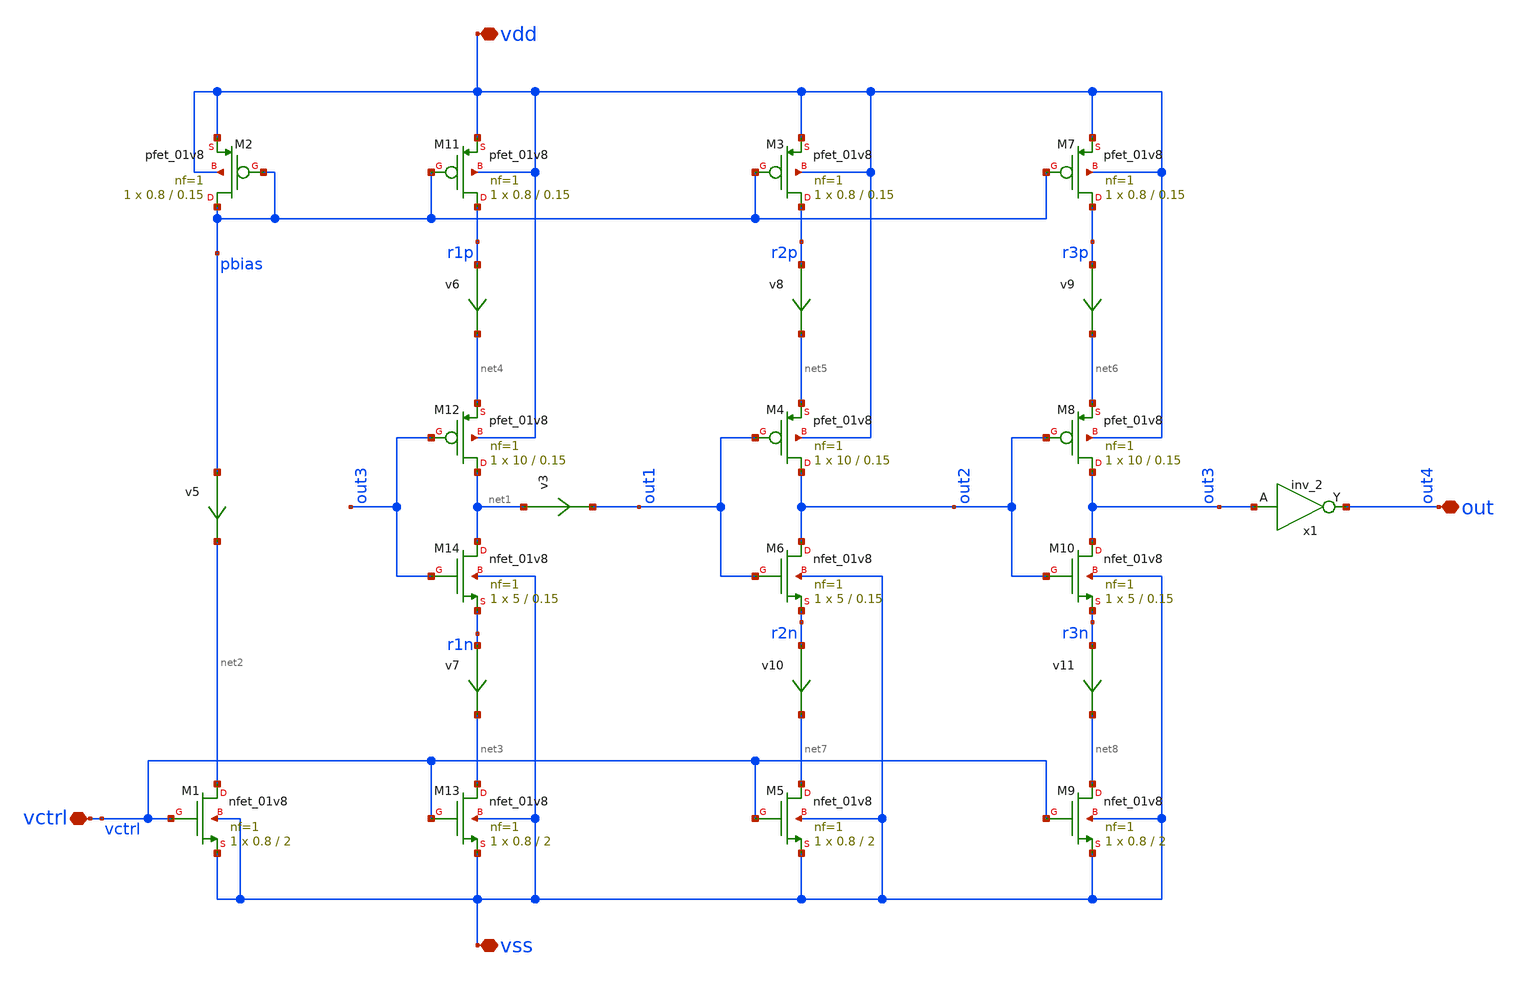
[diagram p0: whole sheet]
** sch_path: xschem/vco/untitled.sch
**.subckt untitled vdd vss vctrl out
*.iopin vdd
*.iopin vss
*.iopin vctrl
*.iopin out
XM1 net2 vctrl vss vss sky130_fd_pr__nfet_01v8 L=2 W=0.8 nf=1 ad='int((nf+1)/2) * W/nf * 0.29' as='int((nf+2)/2) * W/nf * 0.29'
+ pd='2*int((nf+1)/2) * (W/nf + 0.29)' ps='2*int((nf+2)/2) * (W/nf + 0.29)' nrd='0.29 / W' nrs='0.29 / W'
+ sa=0 sb=0 sd=0 mult=1 m=1
XM2 pbias pbias vdd vdd sky130_fd_pr__pfet_01v8 L=0.15 W=0.8 nf=1 ad='int((nf+1)/2) * W/nf * 0.29' as='int((nf+2)/2) * W/nf * 0.29'
+ pd='2*int((nf+1)/2) * (W/nf + 0.29)' ps='2*int((nf+2)/2) * (W/nf + 0.29)' nrd='0.29 / W' nrs='0.29 / W'
+ sa=0 sb=0 sd=0 mult=1 m=1
XM11 r1p pbias vdd vdd sky130_fd_pr__pfet_01v8 L=0.15 W=0.8 nf=1 ad='int((nf+1)/2) * W/nf * 0.29' as='int((nf+2)/2) * W/nf * 0.29'
+ pd='2*int((nf+1)/2) * (W/nf + 0.29)' ps='2*int((nf+2)/2) * (W/nf + 0.29)' nrd='0.29 / W' nrs='0.29 / W'
+ sa=0 sb=0 sd=0 mult=1 m=1
XM12 net1 out3 net4 vdd sky130_fd_pr__pfet_01v8 L=0.15 W=10 nf=1 ad='int((nf+1)/2) * W/nf * 0.29' as='int((nf+2)/2) * W/nf * 0.29'
+ pd='2*int((nf+1)/2) * (W/nf + 0.29)' ps='2*int((nf+2)/2) * (W/nf + 0.29)' nrd='0.29 / W' nrs='0.29 / W'
+ sa=0 sb=0 sd=0 mult=1 m=1
XM13 net3 vctrl vss vss sky130_fd_pr__nfet_01v8 L=2 W=0.8 nf=1 ad='int((nf+1)/2) * W/nf * 0.29' as='int((nf+2)/2) * W/nf * 0.29'
+ pd='2*int((nf+1)/2) * (W/nf + 0.29)' ps='2*int((nf+2)/2) * (W/nf + 0.29)' nrd='0.29 / W' nrs='0.29 / W'
+ sa=0 sb=0 sd=0 mult=1 m=1
XM14 net1 out3 r1n vss sky130_fd_pr__nfet_01v8 L=0.15 W=5 nf=1 ad='int((nf+1)/2) * W/nf * 0.29' as='int((nf+2)/2) * W/nf * 0.29'
+ pd='2*int((nf+1)/2) * (W/nf + 0.29)' ps='2*int((nf+2)/2) * (W/nf + 0.29)' nrd='0.29 / W' nrs='0.29 / W'
+ sa=0 sb=0 sd=0 mult=1 m=1
x1 out3 vss vss vdd vdd out4 sky130_fd_sc_hd__inv_2
v3 net1 out1 0
.save i(v3)
v5 pbias net2 0
.save i(v5)
XM3 r2p pbias vdd vdd sky130_fd_pr__pfet_01v8 L=0.15 W=0.8 nf=1 ad='int((nf+1)/2) * W/nf * 0.29' as='int((nf+2)/2) * W/nf * 0.29'
+ pd='2*int((nf+1)/2) * (W/nf + 0.29)' ps='2*int((nf+2)/2) * (W/nf + 0.29)' nrd='0.29 / W' nrs='0.29 / W'
+ sa=0 sb=0 sd=0 mult=1 m=1
XM4 out2 out1 net5 vdd sky130_fd_pr__pfet_01v8 L=0.15 W=10 nf=1 ad='int((nf+1)/2) * W/nf * 0.29' as='int((nf+2)/2) * W/nf * 0.29'
+ pd='2*int((nf+1)/2) * (W/nf + 0.29)' ps='2*int((nf+2)/2) * (W/nf + 0.29)' nrd='0.29 / W' nrs='0.29 / W'
+ sa=0 sb=0 sd=0 mult=1 m=1
XM5 net7 vctrl vss vss sky130_fd_pr__nfet_01v8 L=2 W=0.8 nf=1 ad='int((nf+1)/2) * W/nf * 0.29' as='int((nf+2)/2) * W/nf * 0.29'
+ pd='2*int((nf+1)/2) * (W/nf + 0.29)' ps='2*int((nf+2)/2) * (W/nf + 0.29)' nrd='0.29 / W' nrs='0.29 / W'
+ sa=0 sb=0 sd=0 mult=1 m=1
XM6 out2 out1 r2n vss sky130_fd_pr__nfet_01v8 L=0.15 W=5 nf=1 ad='int((nf+1)/2) * W/nf * 0.29' as='int((nf+2)/2) * W/nf * 0.29'
+ pd='2*int((nf+1)/2) * (W/nf + 0.29)' ps='2*int((nf+2)/2) * (W/nf + 0.29)' nrd='0.29 / W' nrs='0.29 / W'
+ sa=0 sb=0 sd=0 mult=1 m=1
XM7 r3p pbias vdd vdd sky130_fd_pr__pfet_01v8 L=0.15 W=0.8 nf=1 ad='int((nf+1)/2) * W/nf * 0.29' as='int((nf+2)/2) * W/nf * 0.29'
+ pd='2*int((nf+1)/2) * (W/nf + 0.29)' ps='2*int((nf+2)/2) * (W/nf + 0.29)' nrd='0.29 / W' nrs='0.29 / W'
+ sa=0 sb=0 sd=0 mult=1 m=1
XM8 out3 out2 net6 vdd sky130_fd_pr__pfet_01v8 L=0.15 W=10 nf=1 ad='int((nf+1)/2) * W/nf * 0.29' as='int((nf+2)/2) * W/nf * 0.29'
+ pd='2*int((nf+1)/2) * (W/nf + 0.29)' ps='2*int((nf+2)/2) * (W/nf + 0.29)' nrd='0.29 / W' nrs='0.29 / W'
+ sa=0 sb=0 sd=0 mult=1 m=1
XM9 net8 vctrl vss vss sky130_fd_pr__nfet_01v8 L=2 W=0.8 nf=1 ad='int((nf+1)/2) * W/nf * 0.29' as='int((nf+2)/2) * W/nf * 0.29'
+ pd='2*int((nf+1)/2) * (W/nf + 0.29)' ps='2*int((nf+2)/2) * (W/nf + 0.29)' nrd='0.29 / W' nrs='0.29 / W'
+ sa=0 sb=0 sd=0 mult=1 m=1
XM10 out3 out2 r3n vss sky130_fd_pr__nfet_01v8 L=0.15 W=5 nf=1 ad='int((nf+1)/2) * W/nf * 0.29' as='int((nf+2)/2) * W/nf * 0.29'
+ pd='2*int((nf+1)/2) * (W/nf + 0.29)' ps='2*int((nf+2)/2) * (W/nf + 0.29)' nrd='0.29 / W' nrs='0.29 / W'
+ sa=0 sb=0 sd=0 mult=1 m=1
v6 r1p net4 0
.save i(v6)
v7 r1n net3 0
.save i(v7)
v8 r2p net5 0
.save i(v8)
v9 r3p net6 0
.save i(v9)
v10 r2n net7 0
.save i(v10)
v11 r3n net8 0
.save i(v11)
**.ends
.end
